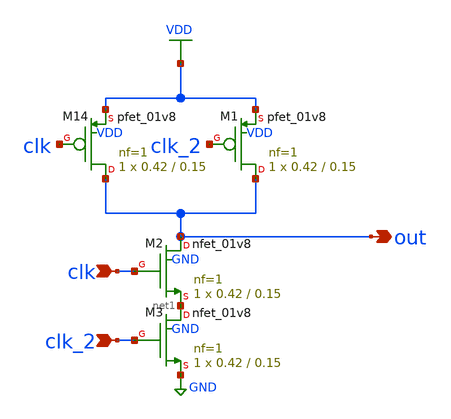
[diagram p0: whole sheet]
** sch_path: xschem/and_set/and_2.sch
**.subckt and_2 clk clk_2 out
*.ipin clk
*.ipin clk_2
*.opin out
XM1 out clk_2 VDD VDD sky130_fd_pr__pfet_01v8 L=0.15 W=0.42 nf=1 ad='int((nf+1)/2) * W/nf * 0.29' as='int((nf+2)/2) * W/nf * 0.29'
+ pd='2*int((nf+1)/2) * (W/nf + 0.29)' ps='2*int((nf+2)/2) * (W/nf + 0.29)' nrd='0.29 / W' nrs='0.29 / W'
+ sa=0 sb=0 sd=0 mult=1 m=1
XM2 out clk net1 GND sky130_fd_pr__nfet_01v8 L=0.15 W=0.42 nf=1 ad='int((nf+1)/2) * W/nf * 0.29' as='int((nf+2)/2) * W/nf * 0.29'
+ pd='2*int((nf+1)/2) * (W/nf + 0.29)' ps='2*int((nf+2)/2) * (W/nf + 0.29)' nrd='0.29 / W' nrs='0.29 / W'
+ sa=0 sb=0 sd=0 mult=1 m=1
XM3 net1 clk_2 GND GND sky130_fd_pr__nfet_01v8 L=0.15 W=0.42 nf=1 ad='int((nf+1)/2) * W/nf * 0.29' as='int((nf+2)/2) * W/nf * 0.29'
+ pd='2*int((nf+1)/2) * (W/nf + 0.29)' ps='2*int((nf+2)/2) * (W/nf + 0.29)' nrd='0.29 / W' nrs='0.29 / W'
+ sa=0 sb=0 sd=0 mult=1 m=1
XM14 out clk VDD VDD sky130_fd_pr__pfet_01v8 L=0.15 W=0.42 nf=1 ad='int((nf+1)/2) * W/nf * 0.29' as='int((nf+2)/2) * W/nf * 0.29'
+ pd='2*int((nf+1)/2) * (W/nf + 0.29)' ps='2*int((nf+2)/2) * (W/nf + 0.29)' nrd='0.29 / W' nrs='0.29 / W'
+ sa=0 sb=0 sd=0 mult=1 m=1
**.ends
.GLOBAL VDD
.GLOBAL GND
.end
